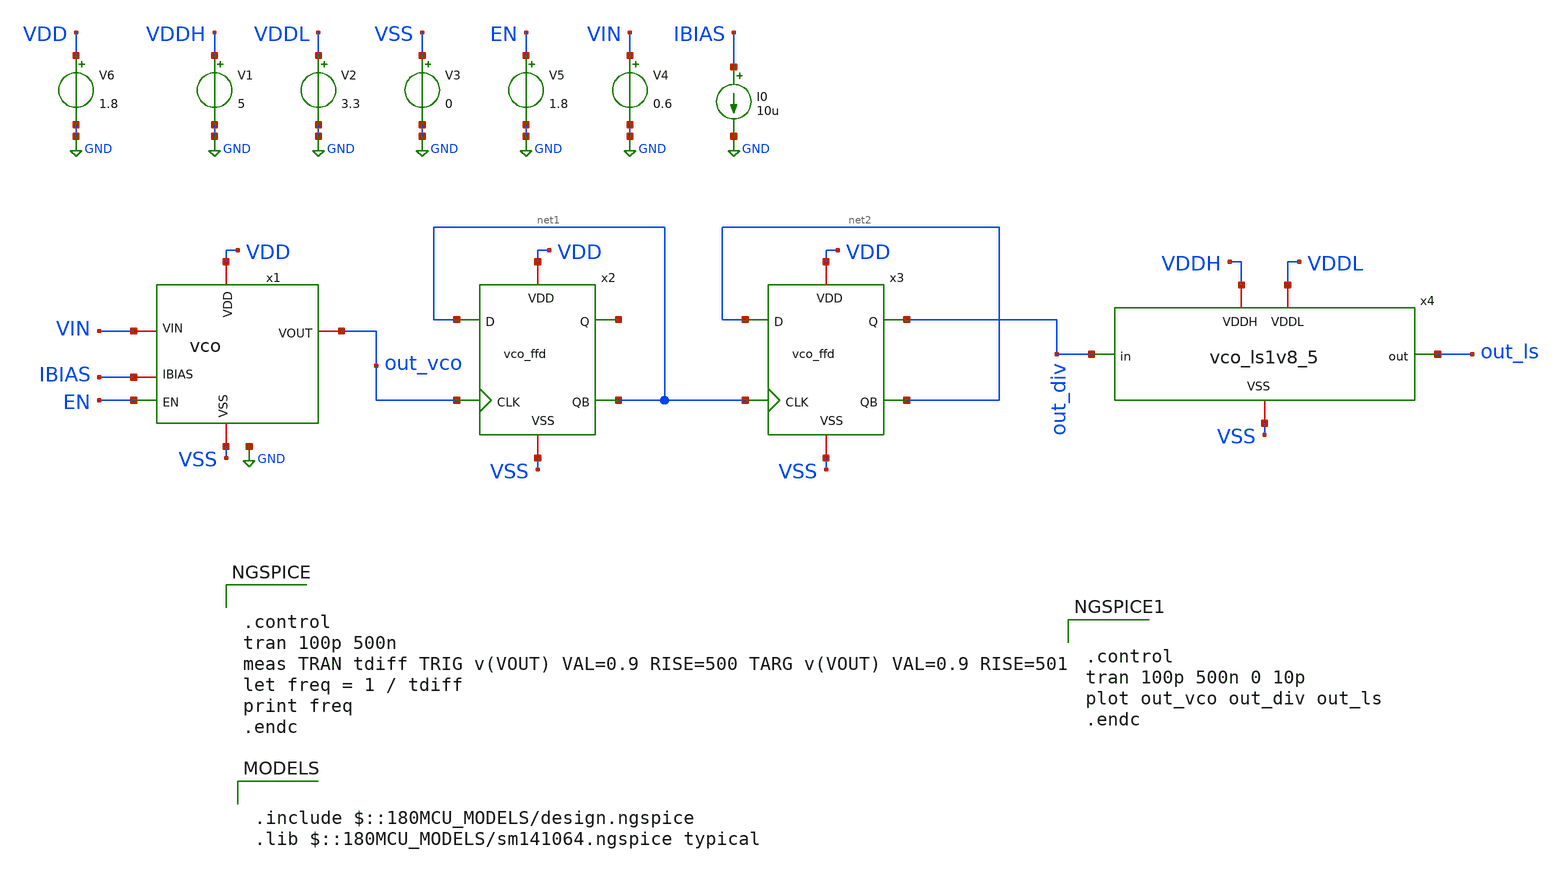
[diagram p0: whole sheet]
** sch_path: designs/libs/tb_vco/tb_vco_div_ls/tb_vco_div_ls.sch
**.subckt tb_vco_div_ls
x1 VDD IBIAS out_vco EN VSS VIN vco
x2 VSS VDD net1 out_vco net3 net1 vco_ffd
x3 VSS VDD net2 net1 out_div net2 vco_ffd
x4 VSS VDDH VDDL out_ls out_div vco_ls1v8_5
V1 VDDH GND 5
V3 VSS GND 0
V2 VDDL GND 3.3
V4 VIN GND 0.6
I0 IBIAS GND 10u
V5 EN GND 1.8
V6 VDD GND 1.8
**** begin user architecture code

.include $::180MCU_MODELS/design.ngspice
.lib $::180MCU_MODELS/sm141064.ngspice typical



.control
tran 100p 500n
meas TRAN tdiff TRIG v(VOUT) VAL=0.9 RISE=500 TARG v(VOUT) VAL=0.9 RISE=501
let freq = 1 / tdiff
print freq
.endc




.control
tran 100p 500n 0 10p
plot out_vco out_div out_ls
.endc


**** end user architecture code
**.ends
.GLOBAL GND
.end
